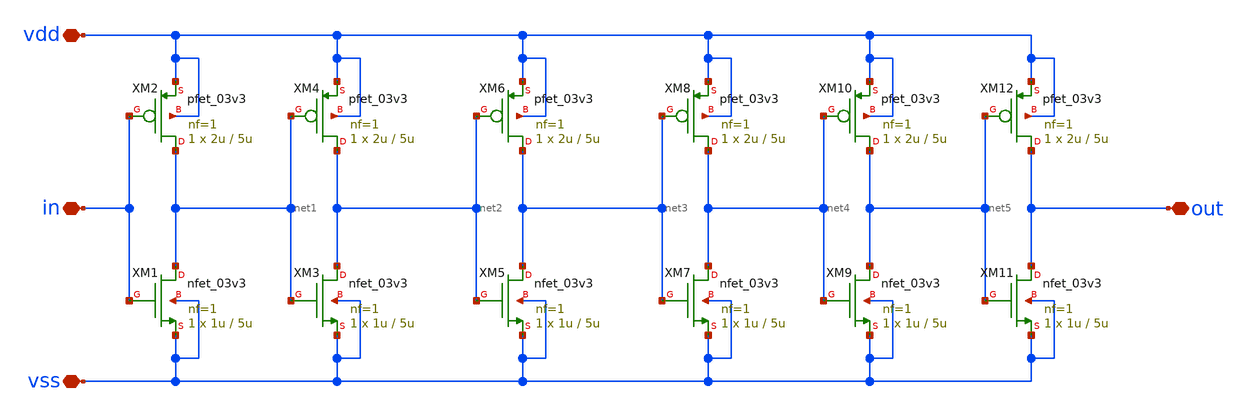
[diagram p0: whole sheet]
** sch_path: designs/libs/qw_core_analog_pkedit/qw_DELAY.sch
**.subckt qw_DELAY vdd vss in out
*.iopin vdd
*.iopin vss
*.iopin in
*.iopin out
XM1 net1 in vss vss nfet_03v3 L=5u W=1u nf=1 ad='int((nf+1)/2) * W/nf * 0.18u' as='int((nf+2)/2) * W/nf * 0.18u'
+ pd='2*int((nf+1)/2) * (W/nf + 0.18u)' ps='2*int((nf+2)/2) * (W/nf + 0.18u)' nrd='0.18u / W' nrs='0.18u / W'
+ sa=0 sb=0 sd=0 m=1
XM2 net1 in vdd vdd pfet_03v3 L=5u W=2u nf=1 ad='int((nf+1)/2) * W/nf * 0.18u' as='int((nf+2)/2) * W/nf * 0.18u'
+ pd='2*int((nf+1)/2) * (W/nf + 0.18u)' ps='2*int((nf+2)/2) * (W/nf + 0.18u)' nrd='0.18u / W' nrs='0.18u / W'
+ sa=0 sb=0 sd=0 m=1
XM3 net2 net1 vss vss nfet_03v3 L=5u W=1u nf=1 ad='int((nf+1)/2) * W/nf * 0.18u' as='int((nf+2)/2) * W/nf * 0.18u'
+ pd='2*int((nf+1)/2) * (W/nf + 0.18u)' ps='2*int((nf+2)/2) * (W/nf + 0.18u)' nrd='0.18u / W' nrs='0.18u / W'
+ sa=0 sb=0 sd=0 m=1
XM4 net2 net1 vdd vdd pfet_03v3 L=5u W=2u nf=1 ad='int((nf+1)/2) * W/nf * 0.18u' as='int((nf+2)/2) * W/nf * 0.18u'
+ pd='2*int((nf+1)/2) * (W/nf + 0.18u)' ps='2*int((nf+2)/2) * (W/nf + 0.18u)' nrd='0.18u / W' nrs='0.18u / W'
+ sa=0 sb=0 sd=0 m=1
XM5 net3 net2 vss vss nfet_03v3 L=5u W=1u nf=1 ad='int((nf+1)/2) * W/nf * 0.18u' as='int((nf+2)/2) * W/nf * 0.18u'
+ pd='2*int((nf+1)/2) * (W/nf + 0.18u)' ps='2*int((nf+2)/2) * (W/nf + 0.18u)' nrd='0.18u / W' nrs='0.18u / W'
+ sa=0 sb=0 sd=0 m=1
XM6 net3 net2 vdd vdd pfet_03v3 L=5u W=2u nf=1 ad='int((nf+1)/2) * W/nf * 0.18u' as='int((nf+2)/2) * W/nf * 0.18u'
+ pd='2*int((nf+1)/2) * (W/nf + 0.18u)' ps='2*int((nf+2)/2) * (W/nf + 0.18u)' nrd='0.18u / W' nrs='0.18u / W'
+ sa=0 sb=0 sd=0 m=1
XM7 net4 net3 vss vss nfet_03v3 L=5u W=1u nf=1 ad='int((nf+1)/2) * W/nf * 0.18u' as='int((nf+2)/2) * W/nf * 0.18u'
+ pd='2*int((nf+1)/2) * (W/nf + 0.18u)' ps='2*int((nf+2)/2) * (W/nf + 0.18u)' nrd='0.18u / W' nrs='0.18u / W'
+ sa=0 sb=0 sd=0 m=1
XM8 net4 net3 vdd vdd pfet_03v3 L=5u W=2u nf=1 ad='int((nf+1)/2) * W/nf * 0.18u' as='int((nf+2)/2) * W/nf * 0.18u'
+ pd='2*int((nf+1)/2) * (W/nf + 0.18u)' ps='2*int((nf+2)/2) * (W/nf + 0.18u)' nrd='0.18u / W' nrs='0.18u / W'
+ sa=0 sb=0 sd=0 m=1
XM9 net5 net4 vss vss nfet_03v3 L=5u W=1u nf=1 ad='int((nf+1)/2) * W/nf * 0.18u' as='int((nf+2)/2) * W/nf * 0.18u'
+ pd='2*int((nf+1)/2) * (W/nf + 0.18u)' ps='2*int((nf+2)/2) * (W/nf + 0.18u)' nrd='0.18u / W' nrs='0.18u / W'
+ sa=0 sb=0 sd=0 m=1
XM10 net5 net4 vdd vdd pfet_03v3 L=5u W=2u nf=1 ad='int((nf+1)/2) * W/nf * 0.18u' as='int((nf+2)/2) * W/nf * 0.18u'
+ pd='2*int((nf+1)/2) * (W/nf + 0.18u)' ps='2*int((nf+2)/2) * (W/nf + 0.18u)' nrd='0.18u / W' nrs='0.18u / W'
+ sa=0 sb=0 sd=0 m=1
XM11 out net5 vss vss nfet_03v3 L=5u W=1u nf=1 ad='int((nf+1)/2) * W/nf * 0.18u' as='int((nf+2)/2) * W/nf * 0.18u'
+ pd='2*int((nf+1)/2) * (W/nf + 0.18u)' ps='2*int((nf+2)/2) * (W/nf + 0.18u)' nrd='0.18u / W' nrs='0.18u / W'
+ sa=0 sb=0 sd=0 m=1
XM12 out net5 vdd vdd pfet_03v3 L=5u W=2u nf=1 ad='int((nf+1)/2) * W/nf * 0.18u' as='int((nf+2)/2) * W/nf * 0.18u'
+ pd='2*int((nf+1)/2) * (W/nf + 0.18u)' ps='2*int((nf+2)/2) * (W/nf + 0.18u)' nrd='0.18u / W' nrs='0.18u / W'
+ sa=0 sb=0 sd=0 m=1
**.ends
.end
